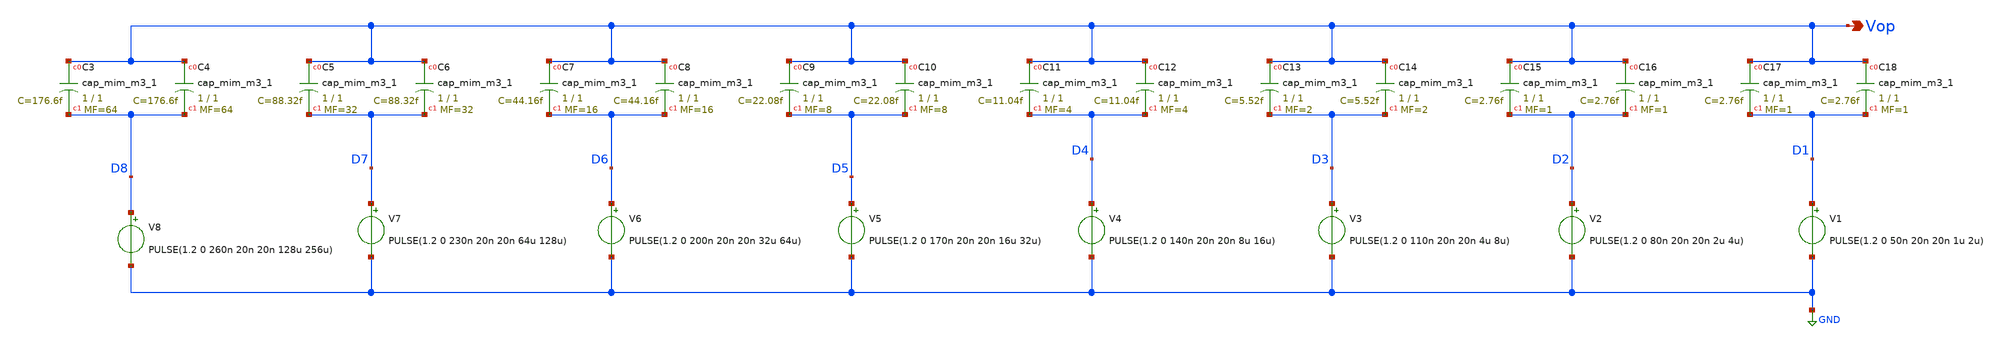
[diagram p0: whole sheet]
** sch_path: C_DAC_Single_ended.sch
**.subckt C_DAC_Single_ended Vop
*.opin Vop
XC3 Vop D8 sky130_fd_pr__cap_mim_m3_1 W=1 L=1 MF=64 m=64
XC4 Vop D8 sky130_fd_pr__cap_mim_m3_1 W=1 L=1 MF=64 m=64
XC5 Vop D7 sky130_fd_pr__cap_mim_m3_1 W=1 L=1 MF=32 m=32
XC6 Vop D7 sky130_fd_pr__cap_mim_m3_1 W=1 L=1 MF=32 m=32
XC7 Vop D6 sky130_fd_pr__cap_mim_m3_1 W=1 L=1 MF=16 m=16
XC8 Vop D6 sky130_fd_pr__cap_mim_m3_1 W=1 L=1 MF=16 m=16
XC9 Vop D5 sky130_fd_pr__cap_mim_m3_1 W=1 L=1 MF=8 m=8
XC10 Vop D5 sky130_fd_pr__cap_mim_m3_1 W=1 L=1 MF=8 m=8
XC11 Vop D4 sky130_fd_pr__cap_mim_m3_1 W=1 L=1 MF=4 m=4
XC12 Vop D4 sky130_fd_pr__cap_mim_m3_1 W=1 L=1 MF=4 m=4
XC13 Vop D3 sky130_fd_pr__cap_mim_m3_1 W=1 L=1 MF=2 m=2
XC14 Vop D3 sky130_fd_pr__cap_mim_m3_1 W=1 L=1 MF=2 m=2
XC15 Vop D2 sky130_fd_pr__cap_mim_m3_1 W=1 L=1 MF=1 m=1
XC16 Vop D2 sky130_fd_pr__cap_mim_m3_1 W=1 L=1 MF=1 m=1
XC17 Vop D1 sky130_fd_pr__cap_mim_m3_1 W=1 L=1 MF=1 m=1
XC18 Vop D1 sky130_fd_pr__cap_mim_m3_1 W=1 L=1 MF=1 m=1
V1 D1 GND PULSE(1.2 0 50n 20n 20n 1u 2u)
V2 D2 GND PULSE(1.2 0 80n 20n 20n 2u 4u)
V3 D3 GND PULSE(1.2 0 110n 20n 20n 4u 8u)
V4 D4 GND PULSE(1.2 0 140n 20n 20n 8u 16u)
V5 D5 GND PULSE(1.2 0 170n 20n 20n 16u 32u)
V6 D6 GND PULSE(1.2 0 200n 20n 20n 32u 64u)
V7 D7 GND PULSE(1.2 0 230n 20n 20n 64u 128u)
V8 D8 GND PULSE(1.2 0 260n 20n 20n 128u 256u)
**** begin user architecture code



.tran 1n 500u
.control
run
plot v(D1)+2 v(D2)+4 v(D3)+6 v(D4)+8 v(D5)+10 v(D6)+12 v(D7)+14 v(D8)+16 v(vop)+18
.endc
.end




** opencircuitdesign pdks install
.lib $::SKYWATER_MODELS/sky130.lib.spice tt

**** end user architecture code
**.ends
.GLOBAL GND
.end
